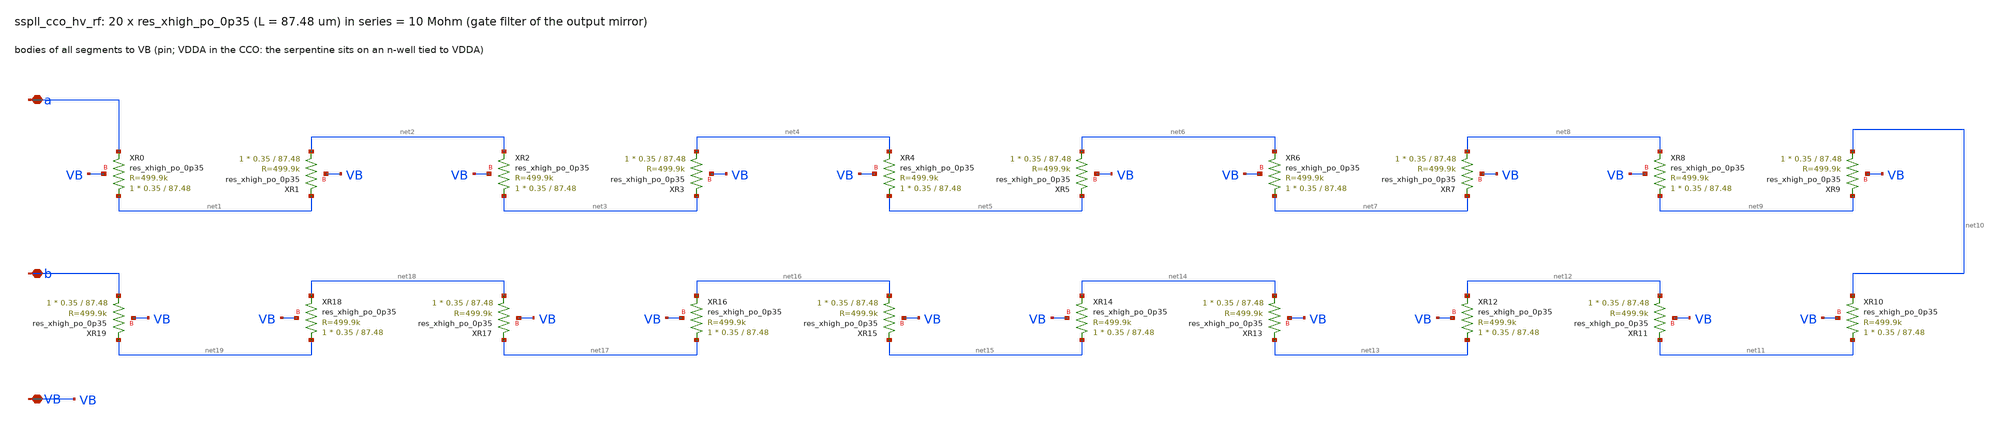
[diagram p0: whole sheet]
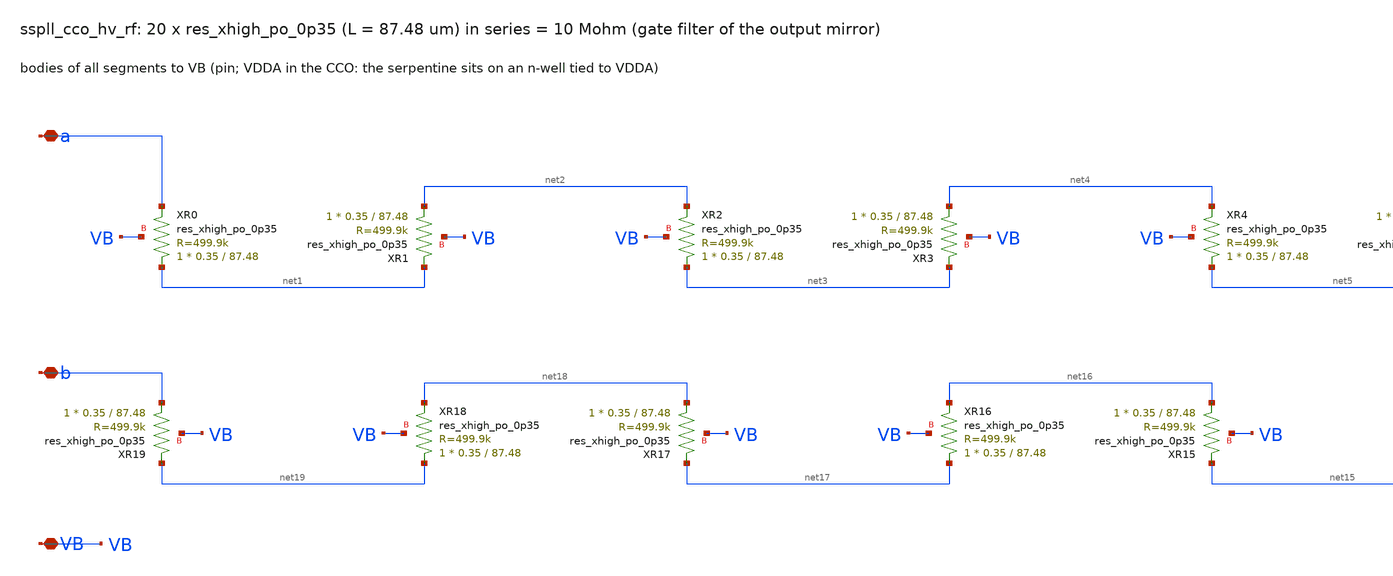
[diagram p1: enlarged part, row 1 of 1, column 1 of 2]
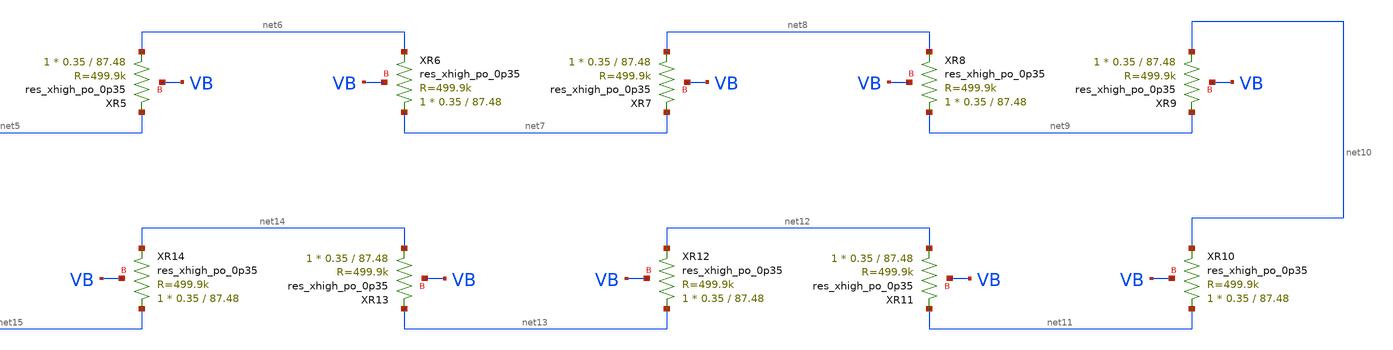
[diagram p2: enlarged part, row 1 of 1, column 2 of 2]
** sch_path: xschem/cco_hv/sspll_cco_hv_rf.sch
**.subckt sspll_cco_hv_rf a b VB
*.iopin a
*.iopin b
*.iopin VB
XXR0 net1 a VB sky130_fd_pr__res_xhigh_po_0p35 L=87.48 mult=1 m=1
XXR1 net2 net1 VB sky130_fd_pr__res_xhigh_po_0p35 L=87.48 mult=1 m=1
XXR2 net3 net2 VB sky130_fd_pr__res_xhigh_po_0p35 L=87.48 mult=1 m=1
XXR3 net4 net3 VB sky130_fd_pr__res_xhigh_po_0p35 L=87.48 mult=1 m=1
XXR4 net5 net4 VB sky130_fd_pr__res_xhigh_po_0p35 L=87.48 mult=1 m=1
XXR5 net6 net5 VB sky130_fd_pr__res_xhigh_po_0p35 L=87.48 mult=1 m=1
XXR6 net7 net6 VB sky130_fd_pr__res_xhigh_po_0p35 L=87.48 mult=1 m=1
XXR7 net8 net7 VB sky130_fd_pr__res_xhigh_po_0p35 L=87.48 mult=1 m=1
XXR8 net9 net8 VB sky130_fd_pr__res_xhigh_po_0p35 L=87.48 mult=1 m=1
XXR9 net10 net9 VB sky130_fd_pr__res_xhigh_po_0p35 L=87.48 mult=1 m=1
XXR10 net11 net10 VB sky130_fd_pr__res_xhigh_po_0p35 L=87.48 mult=1 m=1
XXR11 net12 net11 VB sky130_fd_pr__res_xhigh_po_0p35 L=87.48 mult=1 m=1
XXR12 net13 net12 VB sky130_fd_pr__res_xhigh_po_0p35 L=87.48 mult=1 m=1
XXR13 net14 net13 VB sky130_fd_pr__res_xhigh_po_0p35 L=87.48 mult=1 m=1
XXR14 net15 net14 VB sky130_fd_pr__res_xhigh_po_0p35 L=87.48 mult=1 m=1
XXR15 net16 net15 VB sky130_fd_pr__res_xhigh_po_0p35 L=87.48 mult=1 m=1
XXR16 net17 net16 VB sky130_fd_pr__res_xhigh_po_0p35 L=87.48 mult=1 m=1
XXR17 net18 net17 VB sky130_fd_pr__res_xhigh_po_0p35 L=87.48 mult=1 m=1
XXR18 net19 net18 VB sky130_fd_pr__res_xhigh_po_0p35 L=87.48 mult=1 m=1
XXR19 b net19 VB sky130_fd_pr__res_xhigh_po_0p35 L=87.48 mult=1 m=1
**.ends
.end
